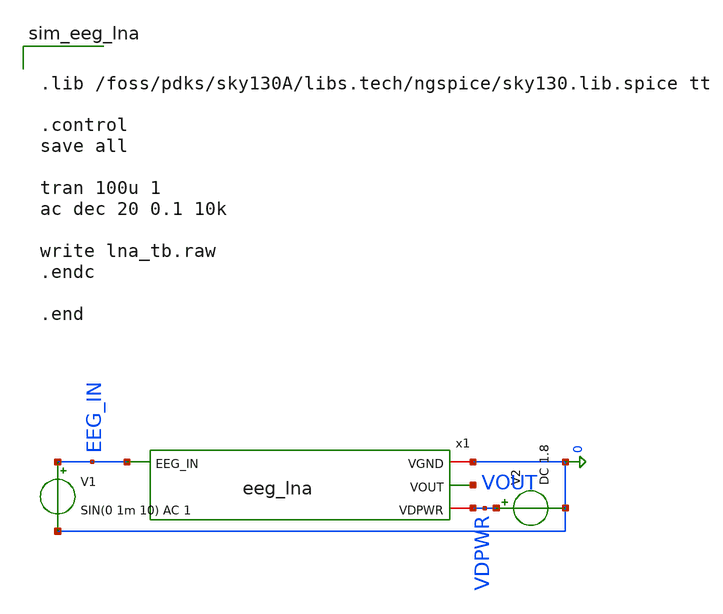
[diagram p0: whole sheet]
** sch_path: xschem/eeg_lna_tb.sch
**.subckt eeg_lna_tb
V1 EEG_IN 0 SIN(0 1m 10) AC 1
V2 VDPWR 0 DC 1.8
x1 EEG_IN 0 VOUT VDPWR eeg_lna
**** begin user architecture code


.lib /foss/pdks/sky130A/libs.tech/ngspice/sky130.lib.spice tt

.control
save all

tran 100u 1
ac dec 20 0.1 10k

write lna_tb.raw
.endc

.end


**** end user architecture code
**.ends

* expanding   symbol:  /foss/designs/ttsky-bci-low-noise-amp/xschem/eeg_lna.sym # of pins=4
** sym_path: xschem/eeg_lna.sym
** sch_path: xschem/eeg_lna.sch
.subckt eeg_lna EEG_IN VGND VOUT VDPWR
*.iopin VGND
*.ipin EEG_IN
*.iopin VDPWR
*.opin VOUT
XM1 MIRROR_BIAS_N MIRROR_BIAS_N VGND VGND sky130_fd_pr__nfet_01v8 L=1.0 W=20 nf=1 ad='int((1 + 1)/2) * 20 / 1 * 0.29'
+ as='int((1 + 2)/2) * 20 / 1 * 0.29' pd='2*int((1 + 1)/2) * (20 / 1 + 0.29)' ps='2*int((1 + 2)/2) * (20 / 1 + 0.29)'
+ nrd='0.29 / 20 ' nrs='0.29 / 20 ' sa=0 sb=0 sd=0 mult=1 m=1
XM2 VOUT MIRROR_BIAS_N VGND VGND sky130_fd_pr__nfet_01v8 L=1.0 W=20 nf=1 ad='int((1 + 1)/2) * 20 / 1 * 0.29'
+ as='int((1 + 2)/2) * 20 / 1 * 0.29' pd='2*int((1 + 1)/2) * (20 / 1 + 0.29)' ps='2*int((1 + 2)/2) * (20 / 1 + 0.29)'
+ nrd='0.29 / 20 ' nrs='0.29 / 20 ' sa=0 sb=0 sd=0 mult=1 m=1
XM3 MIRROR_BIAS_N VIN_P TAIL_P VDPWR sky130_fd_pr__pfet_01v8 L=1.0 W=40 nf=1 ad='int((1 + 1)/2) * 40 / 1 * 0.29'
+ as='int((1 + 2)/2) * 40 / 1 * 0.29' pd='2*int((1 + 1)/2) * (40 / 1 + 0.29)' ps='2*int((1 + 2)/2) * (40 / 1 + 0.29)'
+ nrd='0.29 / 40 ' nrs='0.29 / 40 ' sa=0 sb=0 sd=0 mult=1 m=1
XM4 VOUT VIN_N TAIL_P VDPWR sky130_fd_pr__pfet_01v8 L=1.0 W=40 nf=1 ad='int((1 + 1)/2) * 40 / 1 * 0.29'
+ as='int((1 + 2)/2) * 40 / 1 * 0.29' pd='2*int((1 + 1)/2) * (40 / 1 + 0.29)' ps='2*int((1 + 2)/2) * (40 / 1 + 0.29)'
+ nrd='0.29 / 40 ' nrs='0.29 / 40 ' sa=0 sb=0 sd=0 mult=1 m=1
XM5 TAIL_P BIAS_P VDPWR VDPWR sky130_fd_pr__pfet_01v8 L=1.0 W=30 nf=1 ad='int((1 + 1)/2) * 30 / 1 * 0.29'
+ as='int((1 + 2)/2) * 30 / 1 * 0.29' pd='2*int((1 + 1)/2) * (30 / 1 + 0.29)' ps='2*int((1 + 2)/2) * (30 / 1 + 0.29)'
+ nrd='0.29 / 30 ' nrs='0.29 / 30 ' sa=0 sb=0 sd=0 mult=1 m=1
XM6 BIAS_P BIAS_P VDPWR VDPWR sky130_fd_pr__pfet_01v8 L=1.0 W=10 nf=1 ad='int((1 + 1)/2) * 10 / 1 * 0.29'
+ as='int((1 + 2)/2) * 10 / 1 * 0.29' pd='2*int((1 + 1)/2) * (10 / 1 + 0.29)' ps='2*int((1 + 2)/2) * (10 / 1 + 0.29)'
+ nrd='0.29 / 10 ' nrs='0.29 / 10 ' sa=0 sb=0 sd=0 mult=1 m=1
XM7 BIAS_P BIAS_P VGND VGND sky130_fd_pr__nfet_01v8 L=1.0 W=5 nf=1 ad='int((1 + 1)/2) * 5 / 1 * 0.29'
+ as='int((1 + 2)/2) * 5 / 1 * 0.29' pd='2*int((1 + 1)/2) * (5 / 1 + 0.29)' ps='2*int((1 + 2)/2) * (5 / 1 + 0.29)'
+ nrd='0.29 / 5 ' nrs='0.29 / 5 ' sa=0 sb=0 sd=0 mult=1 m=1
XCIN VIN_P EEG_IN sky130_fd_pr__cap_mim_m3_1 W=100 L=100 MF=1 m=1
RBIAS VIN_P BIAS_P 1Gig m=1
RF VOUT VIN_N 100k m=1
RG VIN_N BIAS_P 100k m=1
.ends

.end
